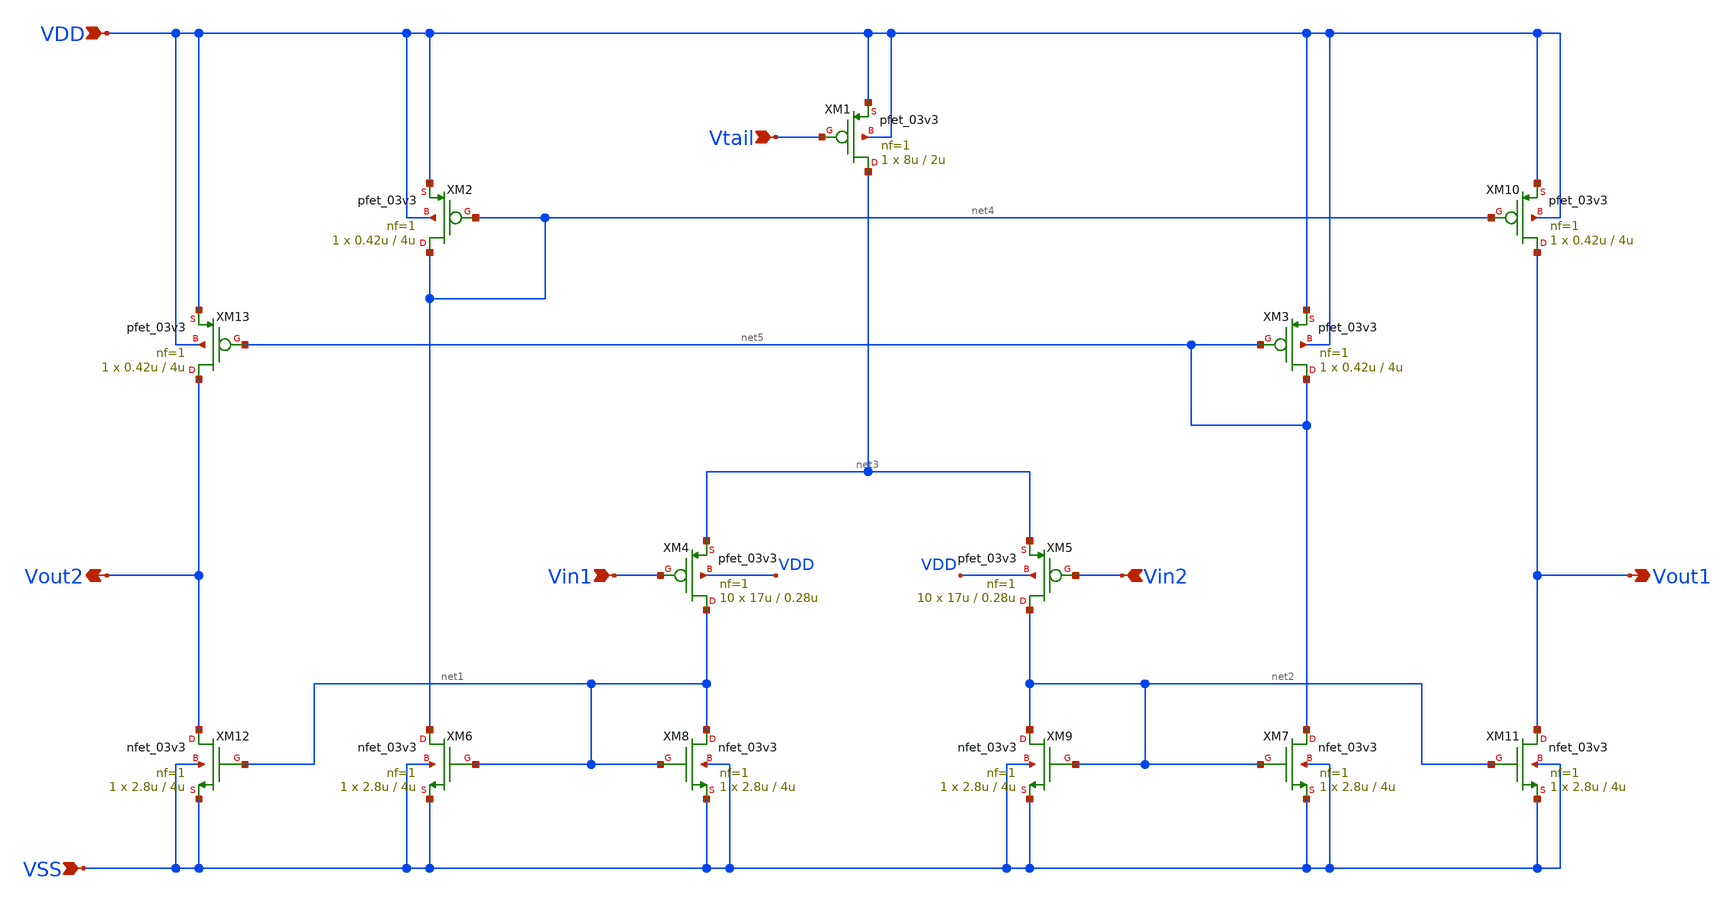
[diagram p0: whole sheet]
** sch_path: designs/libs/core_ina/ina_ota/ina_ota.sch
**.subckt ina_ota Vin1 Vin2 Vtail VSS Vout1 VDD Vout2
*.ipin Vin1
*.ipin Vin2
*.ipin Vtail
*.ipin VSS
*.opin Vout1
*.ipin VDD
*.opin Vout2
XM2 net4 net4 VDD VDD pfet_03v3 L=4u W=0.42u nf=1 ad='int((nf+1)/2) * W/nf * 0.18u' as='int((nf+2)/2) * W/nf * 0.18u'
+ pd='2*int((nf+1)/2) * (W/nf + 0.18u)' ps='2*int((nf+2)/2) * (W/nf + 0.18u)' nrd='0.18u / W' nrs='0.18u / W'
+ sa=0 sb=0 sd=0 m=1
XM1 net3 Vtail VDD VDD pfet_03v3 L=2u W=8u nf=1 ad='int((nf+1)/2) * W/nf * 0.18u' as='int((nf+2)/2) * W/nf * 0.18u'
+ pd='2*int((nf+1)/2) * (W/nf + 0.18u)' ps='2*int((nf+2)/2) * (W/nf + 0.18u)' nrd='0.18u / W' nrs='0.18u / W'
+ sa=0 sb=0 sd=0 m=1
XM3 net5 net5 VDD VDD pfet_03v3 L=4u W=0.42u nf=1 ad='int((nf+1)/2) * W/nf * 0.18u' as='int((nf+2)/2) * W/nf * 0.18u'
+ pd='2*int((nf+1)/2) * (W/nf + 0.18u)' ps='2*int((nf+2)/2) * (W/nf + 0.18u)' nrd='0.18u / W' nrs='0.18u / W'
+ sa=0 sb=0 sd=0 m=1
XM4 net1 Vin1 net3 VDD pfet_03v3 L=0.28u W=17u nf=1 ad='int((nf+1)/2) * W/nf * 0.18u' as='int((nf+2)/2) * W/nf * 0.18u'
+ pd='2*int((nf+1)/2) * (W/nf + 0.18u)' ps='2*int((nf+2)/2) * (W/nf + 0.18u)' nrd='0.18u / W' nrs='0.18u / W'
+ sa=0 sb=0 sd=0 m=10
XM5 net2 Vin2 net3 VDD pfet_03v3 L=0.28u W=17u nf=1 ad='int((nf+1)/2) * W/nf * 0.18u' as='int((nf+2)/2) * W/nf * 0.18u'
+ pd='2*int((nf+1)/2) * (W/nf + 0.18u)' ps='2*int((nf+2)/2) * (W/nf + 0.18u)' nrd='0.18u / W' nrs='0.18u / W'
+ sa=0 sb=0 sd=0 m=10
XM6 net4 net1 VSS VSS nfet_03v3 L=4u W=2.8u nf=1 ad='int((nf+1)/2) * W/nf * 0.18u' as='int((nf+2)/2) * W/nf * 0.18u'
+ pd='2*int((nf+1)/2) * (W/nf + 0.18u)' ps='2*int((nf+2)/2) * (W/nf + 0.18u)' nrd='0.18u / W' nrs='0.18u / W'
+ sa=0 sb=0 sd=0 m=1
XM7 net5 net2 VSS VSS nfet_03v3 L=4u W=2.8u nf=1 ad='int((nf+1)/2) * W/nf * 0.18u' as='int((nf+2)/2) * W/nf * 0.18u'
+ pd='2*int((nf+1)/2) * (W/nf + 0.18u)' ps='2*int((nf+2)/2) * (W/nf + 0.18u)' nrd='0.18u / W' nrs='0.18u / W'
+ sa=0 sb=0 sd=0 m=1
XM8 net1 net1 VSS VSS nfet_03v3 L=4u W=2.8u nf=1 ad='int((nf+1)/2) * W/nf * 0.18u' as='int((nf+2)/2) * W/nf * 0.18u'
+ pd='2*int((nf+1)/2) * (W/nf + 0.18u)' ps='2*int((nf+2)/2) * (W/nf + 0.18u)' nrd='0.18u / W' nrs='0.18u / W'
+ sa=0 sb=0 sd=0 m=1
XM9 net2 net2 VSS VSS nfet_03v3 L=4u W=2.8u nf=1 ad='int((nf+1)/2) * W/nf * 0.18u' as='int((nf+2)/2) * W/nf * 0.18u'
+ pd='2*int((nf+1)/2) * (W/nf + 0.18u)' ps='2*int((nf+2)/2) * (W/nf + 0.18u)' nrd='0.18u / W' nrs='0.18u / W'
+ sa=0 sb=0 sd=0 m=1
XM10 Vout1 net4 VDD VDD pfet_03v3 L=4u W=0.42u nf=1 ad='int((nf+1)/2) * W/nf * 0.18u' as='int((nf+2)/2) * W/nf * 0.18u'
+ pd='2*int((nf+1)/2) * (W/nf + 0.18u)' ps='2*int((nf+2)/2) * (W/nf + 0.18u)' nrd='0.18u / W' nrs='0.18u / W'
+ sa=0 sb=0 sd=0 m=1
XM11 Vout1 net2 VSS VSS nfet_03v3 L=4u W=2.8u nf=1 ad='int((nf+1)/2) * W/nf * 0.18u' as='int((nf+2)/2) * W/nf * 0.18u'
+ pd='2*int((nf+1)/2) * (W/nf + 0.18u)' ps='2*int((nf+2)/2) * (W/nf + 0.18u)' nrd='0.18u / W' nrs='0.18u / W'
+ sa=0 sb=0 sd=0 m=1
XM12 Vout2 net1 VSS VSS nfet_03v3 L=4u W=2.8u nf=1 ad='int((nf+1)/2) * W/nf * 0.18u' as='int((nf+2)/2) * W/nf * 0.18u'
+ pd='2*int((nf+1)/2) * (W/nf + 0.18u)' ps='2*int((nf+2)/2) * (W/nf + 0.18u)' nrd='0.18u / W' nrs='0.18u / W'
+ sa=0 sb=0 sd=0 m=1
XM13 Vout2 net5 VDD VDD pfet_03v3 L=4u W=0.42u nf=1 ad='int((nf+1)/2) * W/nf * 0.18u' as='int((nf+2)/2) * W/nf * 0.18u'
+ pd='2*int((nf+1)/2) * (W/nf + 0.18u)' ps='2*int((nf+2)/2) * (W/nf + 0.18u)' nrd='0.18u / W' nrs='0.18u / W'
+ sa=0 sb=0 sd=0 m=1
**.ends
.end
